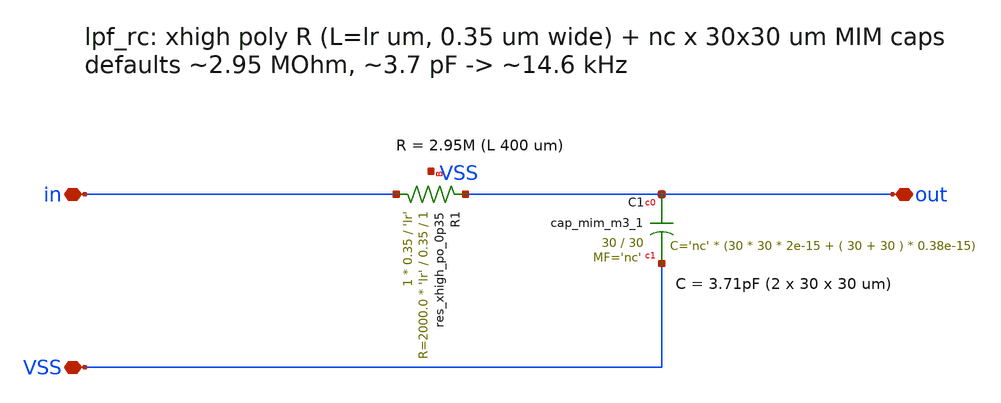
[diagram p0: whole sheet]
** sch_path: xschem/lpf_rc.sch
**.subckt lpf_rc VSS in out
*.iopin VSS
*.iopin in
*.iopin out
XR1 in out VSS sky130_fd_pr__res_xhigh_po_0p35 L='lr' mult=1 m=1
XC1 out VSS sky130_fd_pr__cap_mim_m3_1 W=30 L=30 MF='nc' m='nc'
**.ends
.end
